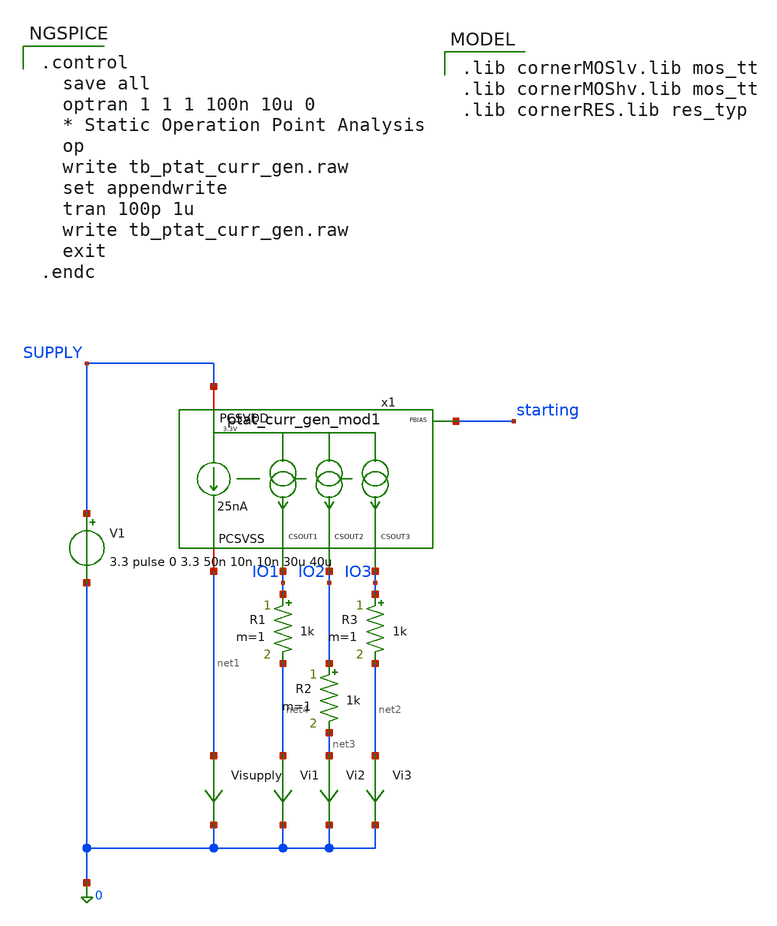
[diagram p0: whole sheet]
** sch_path: macros/heichips26_analog_project/macros/ptat_current_source/testbenches/xschem/tb_ptat_curr_gen.sch
**.subckt tb_ptat_curr_gen
V1 SUPPLY 0 3.3 pulse 0 3.3 50n 10n 10n 30u 40u
R2 IO2 net3 1k m=1
R1 IO1 net4 1k m=1
R3 IO3 net2 1k m=1
Vi1 net4 0 0
.save i(vi1)
Vi2 net3 0 0
.save i(vi2)
Vi3 net2 0 0
.save i(vi3)
Visupply net1 0 0
.save i(visupply)
x1 SUPPLY IO1 IO2 IO3 starting net1 ptat_curr_gen_mod1
**** begin user architecture code

.control
  save all
  optran 1 1 1 100n 10u 0
  * Static Operation Point Analysis
  op
  write tb_ptat_curr_gen.raw
  set appendwrite
  tran 100p 1u
  write tb_ptat_curr_gen.raw
  exit
.endc



.lib cornerMOSlv.lib mos_tt
.lib cornerMOShv.lib mos_tt
.lib cornerRES.lib res_typ


**** end user architecture code
**.ends

* expanding   symbol:  ptat_curr_gen_mod1.sym # of pins=6
** sym_path: macros/heichips26_analog_project/macros/ptat_current_source/schematic/xschem/ptat_curr_gen_mod1.sym
** sch_path: macros/heichips26_analog_project/macros/ptat_current_source/schematic/xschem/ptat_curr_gen_mod1.sch
.subckt ptat_curr_gen_mod1 PCSVDD CSOUT1 CSOUT2 CSOUT3 PBIAS PCSVSS
*.iopin PCSVDD
*.iopin PCSVSS
*.opin CSOUT1
*.opin CSOUT2
*.opin CSOUT3
*.opin PBIAS
XM1 net1 net1 PCSVSS PCSVSS sg13_hv_nmos w=2u l=2u ng=1 m=1 mm_ok=1
XM2 PBIAS net1 res_tap PCSVSS sg13_hv_nmos w=10u l=2u ng=1 m=1 mm_ok=1
XM3 net1 PBIAS PCSVDD PCSVDD sg13_hv_pmos w=0.4u l=1u ng=1 m=1 mm_ok=1
XM4 PBIAS PBIAS PCSVDD PCSVDD sg13_hv_pmos w=0.4u l=1u ng=1 m=1 mm_ok=1
XR1 res_tap PCSVSS PCSVSS rhigh w=0.5e-6 l=30e-6 m=1 b=21 mm_ok=1
XM5 CSOUT3 PBIAS PCSVDD PCSVDD sg13_hv_pmos w=0.4u l=1u ng=1 m=1 mm_ok=1
XM6 CSOUT2 PBIAS PCSVDD PCSVDD sg13_hv_pmos w=0.4u l=1u ng=1 m=1 mm_ok=1
XM7 CSOUT1 PBIAS PCSVDD PCSVDD sg13_hv_pmos w=0.4u l=1u ng=1 m=1 mm_ok=1
XMD1 PCSVSS PCSVSS PCSVSS PCSVSS sg13_hv_nmos w=10u l=2u ng=1 m=1 mm_ok=1
XMD2 PCSVSS PCSVSS PCSVSS PCSVSS sg13_hv_nmos w=10u l=2u ng=1 m=1 mm_ok=1
XMD3 PCSVSS PCSVSS PCSVSS PCSVSS sg13_hv_nmos w=5u l=2u ng=1 m=1 mm_ok=1
XMD4 PCSVSS PCSVSS PCSVSS PCSVSS sg13_hv_nmos w=5u l=2u ng=1 m=1 mm_ok=1
XMD5 PCSVSS PCSVSS PCSVSS PCSVSS sg13_hv_nmos w=5u l=2u ng=1 m=1 mm_ok=1
XMD6 PCSVSS PCSVSS PCSVSS PCSVSS sg13_hv_nmos w=5u l=2u ng=1 m=1 mm_ok=1
XMD7 PCSVSS PCSVSS PCSVSS PCSVSS sg13_hv_nmos w=5u l=2u ng=1 m=1 mm_ok=1
XMD8 PCSVSS PCSVSS PCSVSS PCSVSS sg13_hv_nmos w=5u l=2u ng=1 m=1 mm_ok=1
XMD9 PCSVSS PCSVSS PCSVSS PCSVSS sg13_hv_nmos w=2u l=2u ng=1 m=1 mm_ok=1
XMD10 PCSVSS PCSVSS PCSVSS PCSVSS sg13_hv_nmos w=2u l=2u ng=1 m=1 mm_ok=1
XMD11 PCSVSS PCSVSS PCSVSS PCSVSS sg13_hv_nmos w=1u l=2u ng=1 m=1 mm_ok=1
XMD12 PCSVSS PCSVSS PCSVSS PCSVSS sg13_hv_nmos w=1u l=2u ng=1 m=1 mm_ok=1
XMD13 PCSVSS PCSVSS PCSVSS PCSVSS sg13_hv_nmos w=1u l=2u ng=1 m=1 mm_ok=1
XMD14 PCSVSS PCSVSS PCSVSS PCSVSS sg13_hv_nmos w=1u l=2u ng=1 m=1 mm_ok=1
XMD15 PCSVSS PCSVSS PCSVSS PCSVSS sg13_hv_nmos w=1u l=2u ng=1 m=1 mm_ok=1
XMD16 PCSVSS PCSVSS PCSVSS PCSVSS sg13_hv_nmos w=1u l=2u ng=1 m=1 mm_ok=1
XMD17 PCSVDD PCSVDD PCSVDD PCSVDD sg13_hv_pmos w=0.4u l=1u ng=1 m=1 mm_ok=1
XMD24 PCSVDD PCSVDD PCSVDD PCSVDD sg13_hv_pmos w=0.4u l=1u ng=1 m=1 mm_ok=1
XMD31 PCSVDD PCSVDD PCSVDD PCSVDD sg13_hv_pmos w=0.4u l=1u ng=1 m=1 mm_ok=1
XMD18 PCSVDD PCSVDD PCSVDD PCSVDD sg13_hv_pmos w=0.4u l=1u ng=1 m=1 mm_ok=1
XMD19 PCSVDD PCSVDD PCSVDD PCSVDD sg13_hv_pmos w=0.4u l=1u ng=1 m=1 mm_ok=1
XMD20 PCSVDD PCSVDD PCSVDD PCSVDD sg13_hv_pmos w=0.4u l=1u ng=1 m=1 mm_ok=1
XMD21 PCSVDD PCSVDD PCSVDD PCSVDD sg13_hv_pmos w=0.4u l=1u ng=1 m=1 mm_ok=1
XMD22 PCSVDD PCSVDD PCSVDD PCSVDD sg13_hv_pmos w=0.4u l=1u ng=1 m=1 mm_ok=1
XMD23 PCSVDD PCSVDD PCSVDD PCSVDD sg13_hv_pmos w=0.4u l=1u ng=1 m=1 mm_ok=1
XMD25 PCSVDD PCSVDD PCSVDD PCSVDD sg13_hv_pmos w=0.4u l=1u ng=1 m=1 mm_ok=1
XMD26 PCSVDD PCSVDD PCSVDD PCSVDD sg13_hv_pmos w=0.4u l=1u ng=1 m=1 mm_ok=1
XMD27 PCSVDD PCSVDD PCSVDD PCSVDD sg13_hv_pmos w=0.4u l=1u ng=1 m=1 mm_ok=1
XMD28 PCSVDD PCSVDD PCSVDD PCSVDD sg13_hv_pmos w=0.4u l=1u ng=1 m=1 mm_ok=1
XMD29 PCSVDD PCSVDD PCSVDD PCSVDD sg13_hv_pmos w=0.4u l=1u ng=1 m=1 mm_ok=1
XMD30 PCSVDD PCSVDD PCSVDD PCSVDD sg13_hv_pmos w=0.4u l=1u ng=1 m=1 mm_ok=1
XMD32 PCSVDD PCSVDD PCSVDD PCSVDD sg13_hv_pmos w=0.4u l=1u ng=1 m=1 mm_ok=1
XMD33 PCSVDD PCSVDD PCSVDD PCSVDD sg13_hv_pmos w=0.4u l=1u ng=1 m=1 mm_ok=1
XMD34 PCSVDD PCSVDD PCSVDD PCSVDD sg13_hv_pmos w=0.4u l=1u ng=1 m=1 mm_ok=1
XMD35 PCSVDD PCSVDD PCSVDD PCSVDD sg13_hv_pmos w=0.4u l=1u ng=1 m=1 mm_ok=1
XMD36 PCSVDD PCSVDD PCSVDD PCSVDD sg13_hv_pmos w=0.4u l=1u ng=1 m=1 mm_ok=1
XMS1 net3 net2 PCSVDD PCSVDD sg13_hv_pmos w=0.4u l=1u ng=1 m=1 mm_ok=1
XMS3 PCSVSS net3 net2 PCSVDD sg13_hv_pmos w=0.4u l=1u ng=1 m=1 mm_ok=1
XMSS[5] wcs[4] wcs[4] CSSTARTUP CSSTARTUP sg13_hv_pmos w=0.3u l=0.4u ng=1 m=1 mm_ok=1
XMSS[4] wcs[3] wcs[3] wcs[4] wcs[4] sg13_hv_pmos w=0.3u l=0.4u ng=1 m=1 mm_ok=1
XMSS[3] wcs[2] wcs[2] wcs[3] wcs[3] sg13_hv_pmos w=0.3u l=0.4u ng=1 m=1 mm_ok=1
XMSS[2] wcs[1] wcs[1] wcs[2] wcs[2] sg13_hv_pmos w=0.3u l=0.4u ng=1 m=1 mm_ok=1
XMSS[1] PCSVSS PCSVSS wcs[1] wcs[1] sg13_hv_pmos w=0.3u l=0.4u ng=1 m=1 mm_ok=1
.ends

.end
